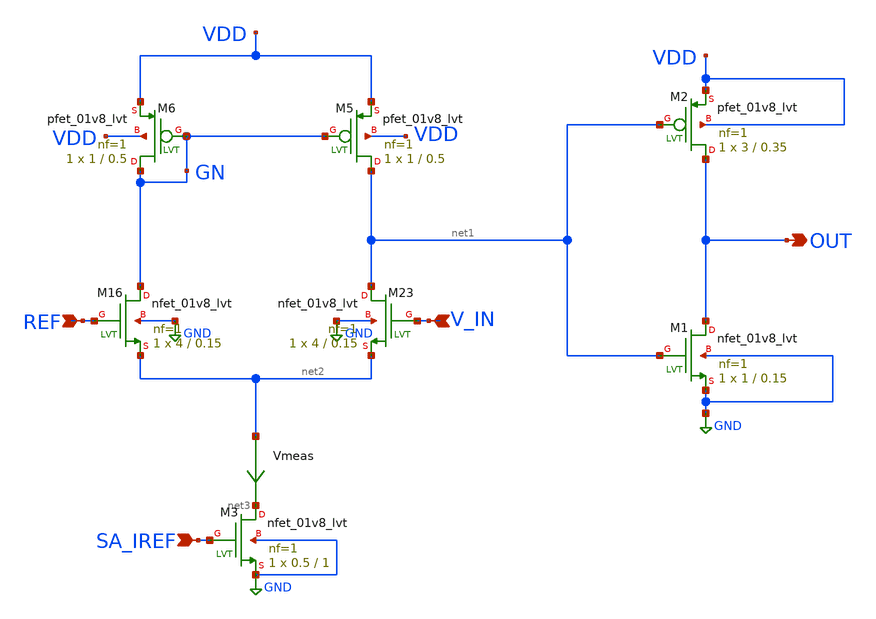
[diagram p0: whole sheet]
** sch_path: xschem/sens_amp.sch
**.subckt sens_amp REF V_IN OUT SA_IREF
*.ipin REF
*.ipin V_IN
*.opin OUT
*.ipin SA_IREF
XM5 net1 GN VDD VDD sky130_fd_pr__pfet_01v8_lvt L=0.5 W=1 nf=1 ad='W * 0.29' as='W * 0.29' pd='2*(W + 0.29)'
+ ps='2*(W + 0.29)' nrd=0 nrs=0 sa=0 sb=0 sd=0 mult=1 m=1
XM6 GN GN VDD VDD sky130_fd_pr__pfet_01v8_lvt L=0.5 W=1 nf=1 ad='W * 0.29' as='W * 0.29' pd='2*(W + 0.29)'
+ ps='2*(W + 0.29)' nrd=0 nrs=0 sa=0 sb=0 sd=0 mult=1 m=1
XM23 net1 V_IN net2 GND sky130_fd_pr__nfet_01v8_lvt L=0.15 W=4 nf=1 ad='W * 0.29' as='W * 0.29' pd='2*(W + 0.29)'
+ ps='2*(W + 0.29)' nrd=0 nrs=0 sa=0 sb=0 sd=0 mult=1 m=1
XM16 GN REF net2 GND sky130_fd_pr__nfet_01v8_lvt L=0.15 W=4 nf=1 ad='W * 0.29' as='W * 0.29' pd='2*(W + 0.29)'
+ ps='2*(W + 0.29)' nrd=0 nrs=0 sa=0 sb=0 sd=0 mult=1 m=1
XM1 OUT net1 GND GND sky130_fd_pr__nfet_01v8_lvt L=0.15 W=1 nf=1 ad='W * 0.29' as='W * 0.29' pd='2*(W + 0.29)'
+ ps='2*(W + 0.29)' nrd=0 nrs=0 sa=0 sb=0 sd=0 mult=1 m=1
XM2 OUT net1 VDD VDD sky130_fd_pr__pfet_01v8_lvt L=0.35 W=3 nf=1 ad='W * 0.29' as='W * 0.29' pd='2*(W + 0.29)'
+ ps='2*(W + 0.29)' nrd=0 nrs=0 sa=0 sb=0 sd=0 mult=1 m=1
XM3 net3 SA_IREF GND GND sky130_fd_pr__nfet_01v8_lvt L=1 W=0.5 nf=1 ad='W * 0.29' as='W * 0.29' pd='2*(W + 0.29)'
+ ps='2*(W + 0.29)' nrd=0 nrs=0 sa=0 sb=0 sd=0 mult=1 m=1
Vmeas net2 net3 0
.save i(vmeas)
**.ends
.GLOBAL GND
.end
